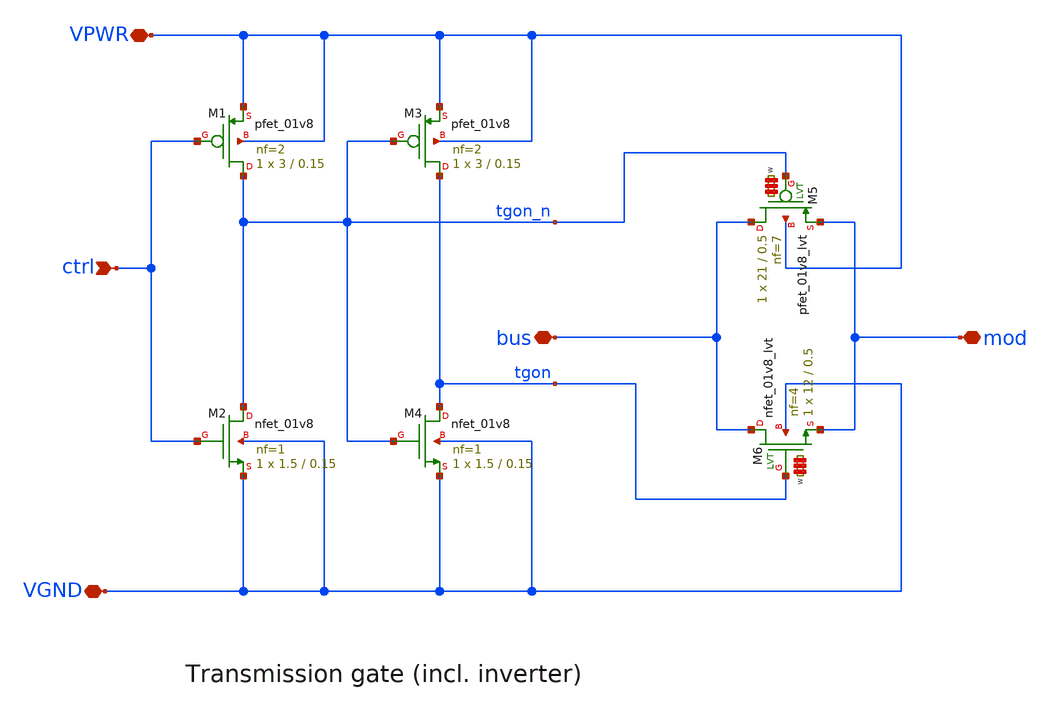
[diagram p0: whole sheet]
** sch_path: xschem/tt_asw_1v8.sch
**.subckt tt_asw_1v8 VPWR VGND mod bus ctrl
*.iopin VPWR
*.iopin VGND
*.iopin mod
*.iopin bus
*.ipin ctrl
XM4 tgon tgon_n VGND VGND sky130_fd_pr__nfet_01v8 L=0.15 W=1.5 nf=1 ad='int((nf+1)/2) * W/nf * 0.29'
+ as='int((nf+2)/2) * W/nf * 0.29' pd='2*int((nf+1)/2) * (W/nf + 0.29)' ps='2*int((nf+2)/2) * (W/nf + 0.29)'
+ nrd='0.29 / W' nrs='0.29 / W' sa=0 sb=0 sd=0 mult=1 m=1
XM3 tgon tgon_n VPWR VPWR sky130_fd_pr__pfet_01v8 L=0.15 W=3 nf=2 ad='int((nf+1)/2) * W/nf * 0.29' as='int((nf+2)/2) * W/nf * 0.29'
+ pd='2*int((nf+1)/2) * (W/nf + 0.29)' ps='2*int((nf+2)/2) * (W/nf + 0.29)' nrd='0.29 / W' nrs='0.29 / W'
+ sa=0 sb=0 sd=0 mult=1 m=1
XM2 tgon_n ctrl VGND VGND sky130_fd_pr__nfet_01v8 L=0.15 W=1.5 nf=1 ad='int((nf+1)/2) * W/nf * 0.29'
+ as='int((nf+2)/2) * W/nf * 0.29' pd='2*int((nf+1)/2) * (W/nf + 0.29)' ps='2*int((nf+2)/2) * (W/nf + 0.29)'
+ nrd='0.29 / W' nrs='0.29 / W' sa=0 sb=0 sd=0 mult=1 m=1
XM1 tgon_n ctrl VPWR VPWR sky130_fd_pr__pfet_01v8 L=0.15 W=3 nf=2 ad='int((nf+1)/2) * W/nf * 0.29' as='int((nf+2)/2) * W/nf * 0.29'
+ pd='2*int((nf+1)/2) * (W/nf + 0.29)' ps='2*int((nf+2)/2) * (W/nf + 0.29)' nrd='0.29 / W' nrs='0.29 / W'
+ sa=0 sb=0 sd=0 mult=1 m=1
XM6 bus tgon mod VGND sky130_fd_pr__nfet_01v8_lvt L=0.5 W='12 * 4 ' nf=4 ad='int((nf+1)/2) * W / nf * 0.29'
+ as='int((nf+2)/2) * W / nf * 0.29' pd='2*int((nf+1)/2) * (W / nf + 0.29)' ps='2*int((nf+2)/2) * (W / nf + 0.29)'
+ nrd='0.29 / W ' nrs='0.29 / W ' sa=0 sb=0 sd=0 mult=1 m=1
XM5 bus tgon_n mod VPWR sky130_fd_pr__pfet_01v8_lvt L=0.5 W='21 * 7 ' nf=7 ad='int((nf+1)/2) * W / nf * 0.29'
+ as='int((nf+2)/2) * W / nf * 0.29' pd='2*int((nf+1)/2) * (W / nf + 0.29)' ps='2*int((nf+2)/2) * (W / nf + 0.29)'
+ nrd='0.29 / W ' nrs='0.29 / W ' sa=0 sb=0 sd=0 mult=1 m=1
**.ends
.end
